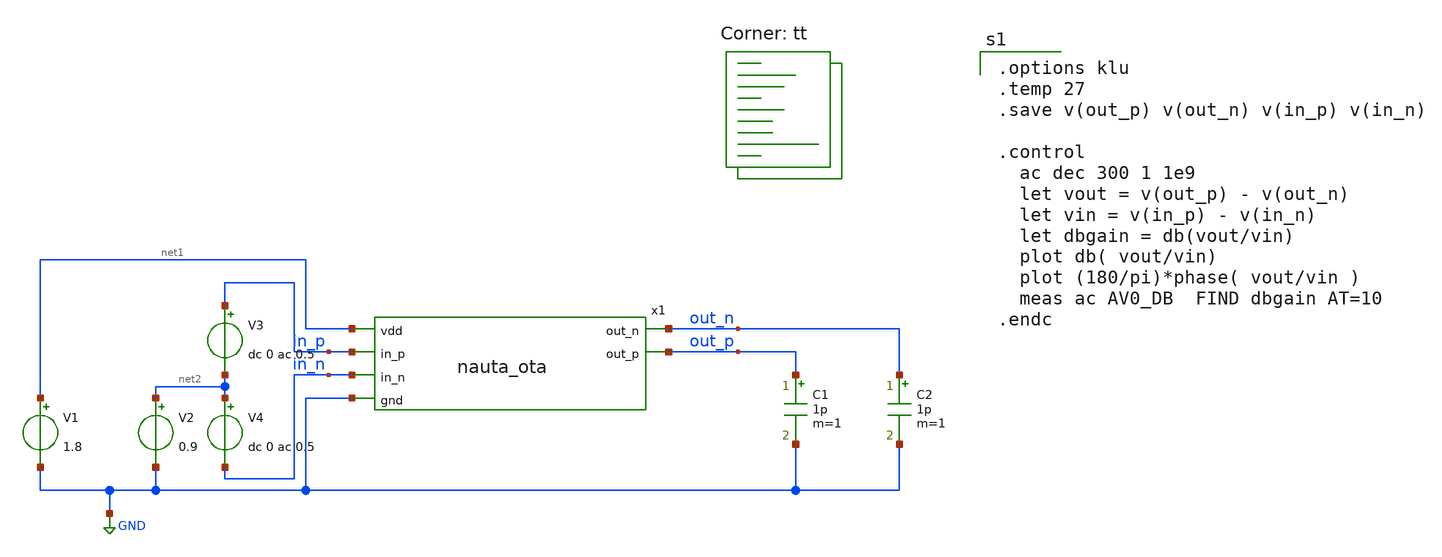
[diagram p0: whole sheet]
** sch_path: xsch/nauta_ota_tb.sch
**.subckt nauta_ota_tb
V1 net1 GND 1.8
V2 net2 GND 0.9
x1 net1 out_n in_p out_p in_n GND nauta_ota
V3 in_p net2 dc 0 ac 0.5
V4 net2 in_n dc 0 ac 0.5
C1 out_p GND 1p m=1
C2 out_n GND 1p m=1
**** begin user architecture code
.lib $::SKYWATER_MODELS/sky130.lib.spice tt

.options klu
.temp 27
.save v(out_p) v(out_n) v(in_p) v(in_n)

.control
  ac dec 300 1 1e9
  let vout = v(out_p) - v(out_n)
  let vin = v(in_p) - v(in_n)
  let dbgain = db(vout/vin)
  plot db( vout/vin)
  plot (180/pi)*phase( vout/vin )
  meas ac AV0_DB  FIND dbgain AT=10
.endc



**** end user architecture code
**.ends
.GLOBAL GND
.end
